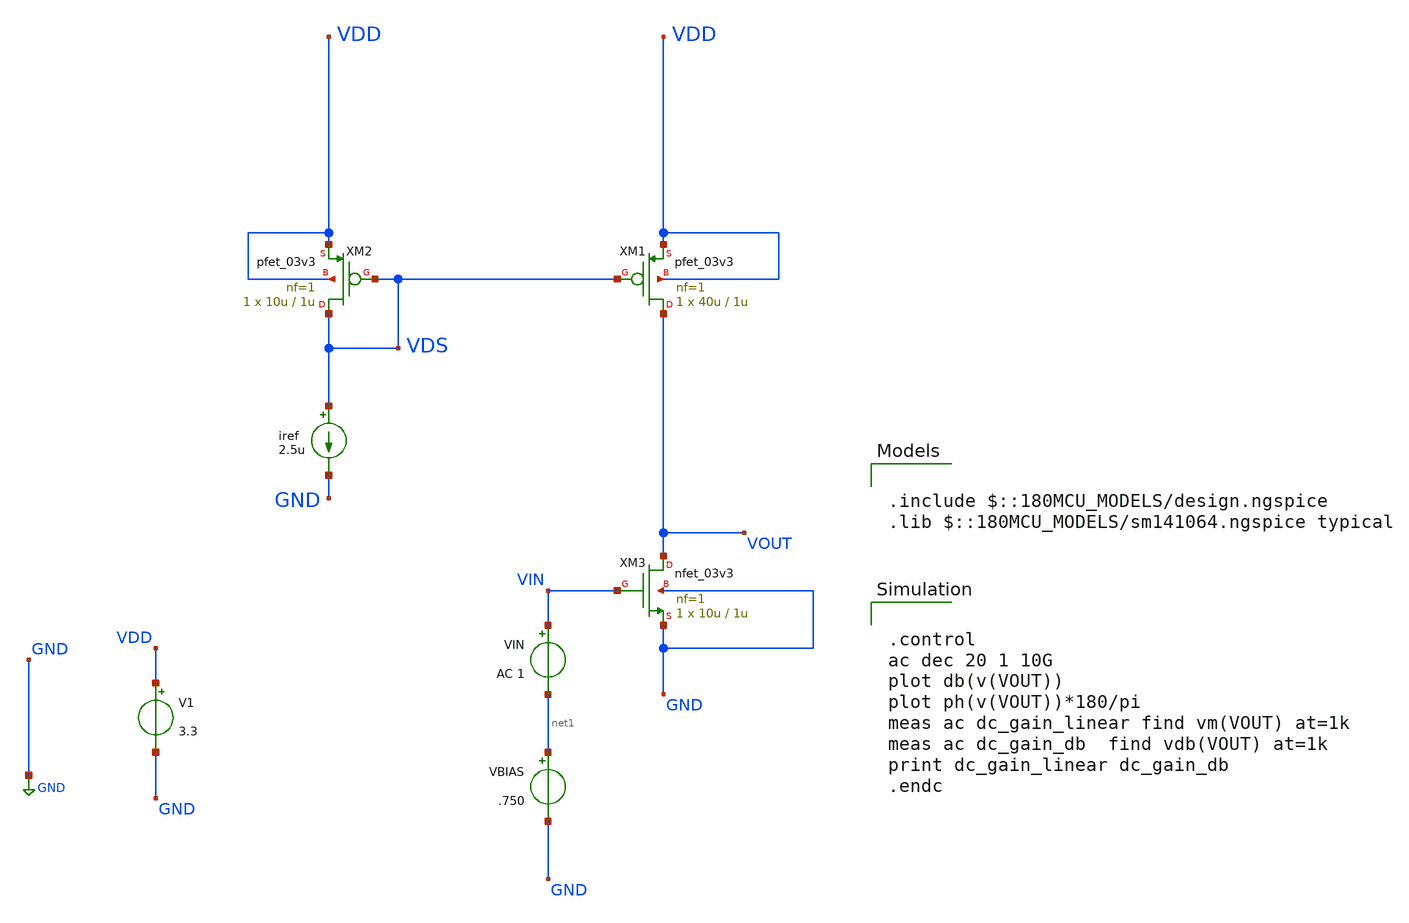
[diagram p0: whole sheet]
** sch_path: designs/libs/session_2/ac_cs_active_load_amp.sch
**.subckt ac_cs_active_load_amp
iref VDS GND 2.5u
XM1 VOUT VDS VDD VDD pfet_03v3 L=1u W=40u nf=1 ad='int((nf+1)/2) * W/nf * 0.18u' as='int((nf+2)/2) * W/nf * 0.18u'
+ pd='2*int((nf+1)/2) * (W/nf + 0.18u)' ps='2*int((nf+2)/2) * (W/nf + 0.18u)' nrd='0.18u / W' nrs='0.18u / W'
+ sa=0 sb=0 sd=0 m=1
XM2 VDS VDS VDD VDD pfet_03v3 L=1u W=10u nf=1 ad='int((nf+1)/2) * W/nf * 0.18u' as='int((nf+2)/2) * W/nf * 0.18u'
+ pd='2*int((nf+1)/2) * (W/nf + 0.18u)' ps='2*int((nf+2)/2) * (W/nf + 0.18u)' nrd='0.18u / W' nrs='0.18u / W'
+ sa=0 sb=0 sd=0 m=1
XM3 VOUT VIN GND GND nfet_03v3 L=1u W=10u nf=1 ad='int((nf+1)/2) * W/nf * 0.18u' as='int((nf+2)/2) * W/nf * 0.18u'
+ pd='2*int((nf+1)/2) * (W/nf + 0.18u)' ps='2*int((nf+2)/2) * (W/nf + 0.18u)' nrd='0.18u / W' nrs='0.18u / W'
+ sa=0 sb=0 sd=0 m=1
V1 VDD GND 3.3
VBIAS net1 GND .750
VIN VIN net1 AC 1
**** begin user architecture code


.control
ac dec 20 1 10G
plot db(v(VOUT))
plot ph(v(VOUT))*180/pi
meas ac dc_gain_linear find vm(VOUT) at=1k
meas ac dc_gain_db  find vdb(VOUT) at=1k
print dc_gain_linear dc_gain_db
.endc



.include $::180MCU_MODELS/design.ngspice
.lib $::180MCU_MODELS/sm141064.ngspice typical

**** end user architecture code
**.ends
.GLOBAL GND
.end
